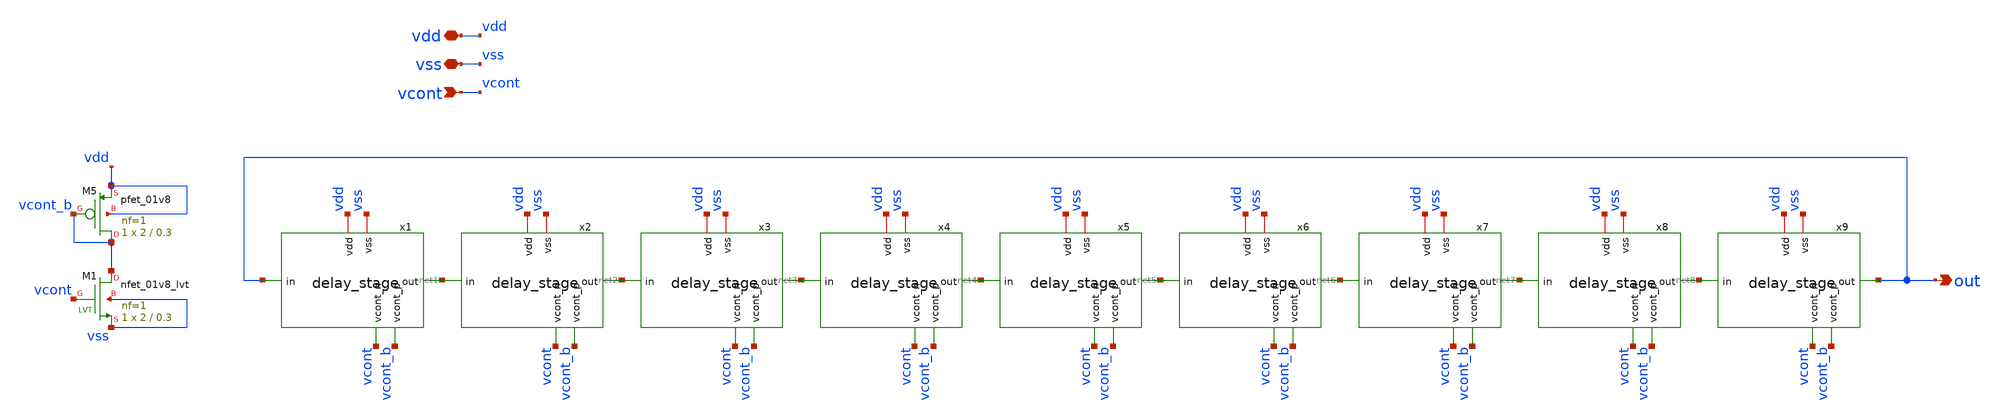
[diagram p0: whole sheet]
** sch_path: xschem/ring_osc9.sch
**.subckt ring_osc9 vdd vcont vss out
*.iopin vdd
*.ipin vcont
*.iopin vss
*.opin out
x1 vdd vcont_b net1 out vcont vss delay_stage
x2 vdd vcont_b net2 net1 vcont vss delay_stage
x3 vdd vcont_b net3 net2 vcont vss delay_stage
XM5 vcont_b vcont_b vdd vdd sky130_fd_pr__pfet_01v8 L=0.3 W=2 nf=1 ad='int((nf+1)/2) * W/nf * 0.29' as='int((nf+2)/2) * W/nf * 0.29'
+ pd='2*int((nf+1)/2) * (W/nf + 0.29)' ps='2*int((nf+2)/2) * (W/nf + 0.29)' nrd='0.29 / W' nrs='0.29 / W'
+ sa=0 sb=0 sd=0 mult=1 m=1
XM1 vcont_b vcont vss vss sky130_fd_pr__nfet_01v8_lvt L=0.3 W=2 nf=1 ad='int((nf+1)/2) * W/nf * 0.29'
+ as='int((nf+2)/2) * W/nf * 0.29' pd='2*int((nf+1)/2) * (W/nf + 0.29)' ps='2*int((nf+2)/2) * (W/nf + 0.29)'
+ nrd='0.29 / W' nrs='0.29 / W' sa=0 sb=0 sd=0 mult=1 m=1
x4 vdd vcont_b net4 net3 vcont vss delay_stage
x5 vdd vcont_b net5 net4 vcont vss delay_stage
x6 vdd vcont_b net6 net5 vcont vss delay_stage
x7 vdd vcont_b net7 net6 vcont vss delay_stage
x8 vdd vcont_b net8 net7 vcont vss delay_stage
x9 vdd vcont_b out net8 vcont vss delay_stage
**.ends

* expanding   symbol:  delay_stage.sym # of pins=6
** sym_path: xschem/delay_stage.sym
** sch_path: xschem/delay_stage.sch
.subckt delay_stage vdd vcont_p out in vcont_n vss
*.ipin in
*.opin out
*.iopin vdd
*.ipin vcont_n
*.ipin vcont_p
*.iopin vss
XM3 out in net2 vss sky130_fd_pr__nfet_01v8 L=0.45 W=1 nf=1 ad='int((nf+1)/2) * W/nf * 0.29' as='int((nf+2)/2) * W/nf * 0.29'
+ pd='2*int((nf+1)/2) * (W/nf + 0.29)' ps='2*int((nf+2)/2) * (W/nf + 0.29)' nrd='0.29 / W' nrs='0.29 / W'
+ sa=0 sb=0 sd=0 mult=1 m=1
XM2 out in net1 vdd sky130_fd_pr__pfet_01v8 L=0.45 W=2 nf=1 ad='int((nf+1)/2) * W/nf * 0.29' as='int((nf+2)/2) * W/nf * 0.29'
+ pd='2*int((nf+1)/2) * (W/nf + 0.29)' ps='2*int((nf+2)/2) * (W/nf + 0.29)' nrd='0.29 / W' nrs='0.29 / W'
+ sa=0 sb=0 sd=0 mult=1 m=1
XM1 net1 vcont_p vdd vdd sky130_fd_pr__pfet_01v8 L=0.45 W=2 nf=1 ad='int((nf+1)/2) * W/nf * 0.29' as='int((nf+2)/2) * W/nf * 0.29'
+ pd='2*int((nf+1)/2) * (W/nf + 0.29)' ps='2*int((nf+2)/2) * (W/nf + 0.29)' nrd='0.29 / W' nrs='0.29 / W'
+ sa=0 sb=0 sd=0 mult=1 m=1
XM4 net2 vcont_n vss vss sky130_fd_pr__nfet_01v8 L=0.45 W=1 nf=1 ad='int((nf+1)/2) * W/nf * 0.29' as='int((nf+2)/2) * W/nf * 0.29'
+ pd='2*int((nf+1)/2) * (W/nf + 0.29)' ps='2*int((nf+2)/2) * (W/nf + 0.29)' nrd='0.29 / W' nrs='0.29 / W'
+ sa=0 sb=0 sd=0 mult=1 m=1
.ends

.end
